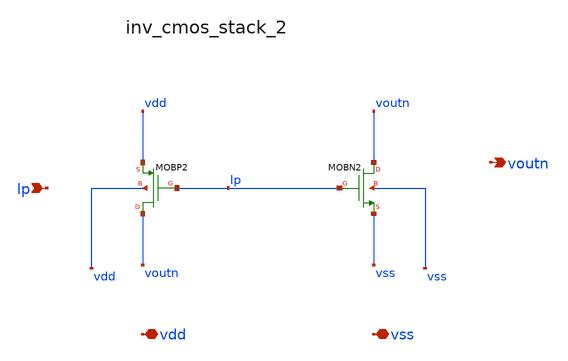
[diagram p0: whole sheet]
** sch_path: analog-db/raw/cmp_002_strongarm/hier/blocks/inv_cmos_stack_2.sch
**.subckt inv_cmos_stack_2 lp vdd vss voutn
*.ipin lp
*.iopin vdd
*.iopin vss
*.opin voutn
XMOBN2 voutn lp vss vss sg13_lv_nmos w=x_dut_xmobn2_w l=x_dut_xmobn2_l ng=1 m=x_dut_xmobn2_m
XMOBP2 voutn lp vdd vdd sg13_lv_pmos w=x_dut_xmobp2_w l=x_dut_xmobp2_l ng=1 m=x_dut_xmobp2_m
**.ends
.end
